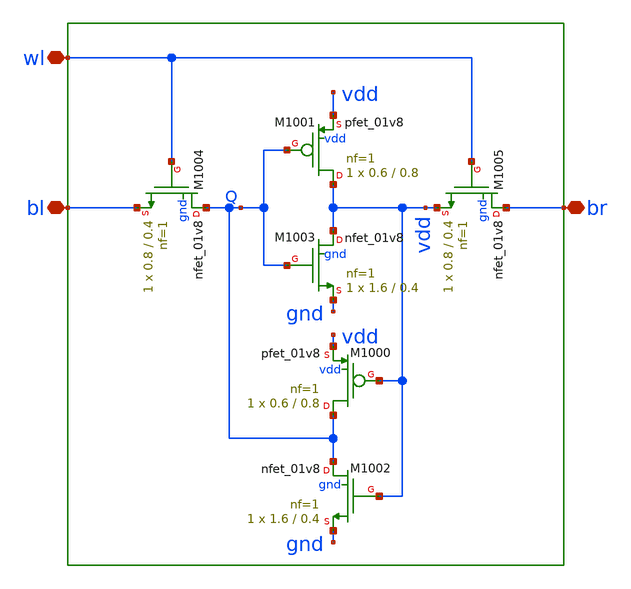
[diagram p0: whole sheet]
** sch_path: sram_4_16_scn4m/replica_cell_1rw.sch
**.subckt replica_cell_1rw bl br wl
*.iopin bl
*.iopin br
*.iopin wl
XM1004 Q wl bl gnd sky130_fd_pr__nfet_01v8 L=0.4 W=0.8 nf=1 ad='int((nf+1)/2) * W/nf * 0.29' as='int((nf+2)/2) * W/nf * 0.29'
+ pd='2*int((nf+1)/2) * (W/nf + 0.29)' ps='2*int((nf+2)/2) * (W/nf + 0.29)' nrd='0.29 / W' nrs='0.29 / W'
+ sa=0 sb=0 sd=0 mult=1 m=1
XM1001 vdd Q vdd vdd sky130_fd_pr__pfet_01v8 L=0.8 W=0.6 nf=1 ad='int((nf+1)/2) * W/nf * 0.29' as='int((nf+2)/2) * W/nf * 0.29'
+ pd='2*int((nf+1)/2) * (W/nf + 0.29)' ps='2*int((nf+2)/2) * (W/nf + 0.29)' nrd='0.29 / W' nrs='0.29 / W'
+ sa=0 sb=0 sd=0 mult=1 m=1
XM1003 vdd Q gnd gnd sky130_fd_pr__nfet_01v8 L=0.4 W=1.6 nf=1 ad='int((nf+1)/2) * W/nf * 0.29' as='int((nf+2)/2) * W/nf * 0.29'
+ pd='2*int((nf+1)/2) * (W/nf + 0.29)' ps='2*int((nf+2)/2) * (W/nf + 0.29)' nrd='0.29 / W' nrs='0.29 / W'
+ sa=0 sb=0 sd=0 mult=1 m=1
XM1002 Q vdd gnd gnd sky130_fd_pr__nfet_01v8 L=0.4 W=1.6 nf=1 ad='int((nf+1)/2) * W/nf * 0.29' as='int((nf+2)/2) * W/nf * 0.29'
+ pd='2*int((nf+1)/2) * (W/nf + 0.29)' ps='2*int((nf+2)/2) * (W/nf + 0.29)' nrd='0.29 / W' nrs='0.29 / W'
+ sa=0 sb=0 sd=0 mult=1 m=1
XM1000 Q vdd vdd vdd sky130_fd_pr__pfet_01v8 L=0.8 W=0.6 nf=1 ad='int((nf+1)/2) * W/nf * 0.29' as='int((nf+2)/2) * W/nf * 0.29'
+ pd='2*int((nf+1)/2) * (W/nf + 0.29)' ps='2*int((nf+2)/2) * (W/nf + 0.29)' nrd='0.29 / W' nrs='0.29 / W'
+ sa=0 sb=0 sd=0 mult=1 m=1
XM1005 br wl vdd gnd sky130_fd_pr__nfet_01v8 L=0.4 W=0.8 nf=1 ad='int((nf+1)/2) * W/nf * 0.29' as='int((nf+2)/2) * W/nf * 0.29'
+ pd='2*int((nf+1)/2) * (W/nf + 0.29)' ps='2*int((nf+2)/2) * (W/nf + 0.29)' nrd='0.29 / W' nrs='0.29 / W'
+ sa=0 sb=0 sd=0 mult=1 m=1
**.ends
.end
